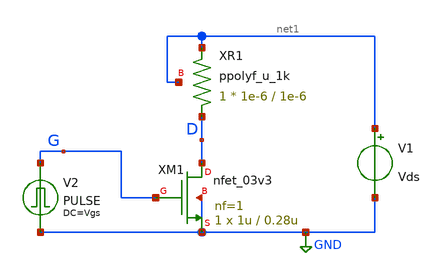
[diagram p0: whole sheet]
** sch_path: gf180mcuD/xschem_libs/gf180mcu_tests/test_nfet_TRAN/schematic/test_nfet_TRAN.sch
**.subckt test_nfet_TRAN
XM1 D G GND GND nfet_03v3 L=0.28u W=1u nf=1 ad='int((nf+1)/2) * W/nf * 0.18u' as='int((nf+2)/2) * W/nf * 0.18u'
+ pd='2*int((nf+1)/2) * (W/nf + 0.18u)' ps='2*int((nf+2)/2) * (W/nf + 0.18u)' nrd='0.18u / W' nrs='0.18u / W'
+ sa=0 sb=0 sd=0 m=1
V1 net1 GND Vds
V2 G GND Vgs PULSE(0 Vgs 10n 1n 1n 50n 100n )
XR1 D net1 net1 ppolyf_u_1k r_width=1e-6 r_length=1e-6 m=1
**.ends
.GLOBAL GND
.end
